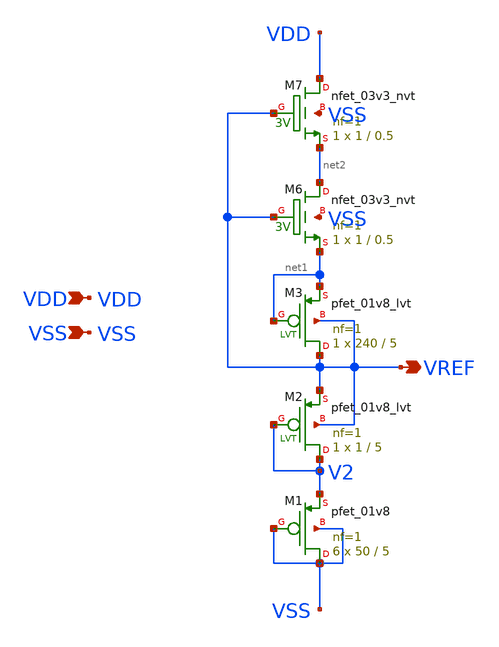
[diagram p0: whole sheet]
** sch_path: design/LELO_SVOD_SKY130A/LELO_SVOD_VTREF.sch
**.subckt LELO_SVOD_VTREF VDD VSS VREF
*.ipin VDD
*.ipin VSS
*.opin VREF
XM1 VSS VSS V2 VSS sky130_fd_pr__pfet_01v8 L=5 W=50 nf=1 ad='int((1 + 1)/2) * 50 / 1 * 0.29' as='int((1 + 2)/2) * 50 / 1 * 0.29'
+ pd='2*int((1 + 1)/2) * (50 / 1 + 0.29)' ps='2*int((1 + 2)/2) * (50 / 1 + 0.29)' nrd='0.29 / 50 ' nrs='0.29 / 50 '
+ sa=0 sb=0 sd=0 mult=6 m=6
XM2 V2 V2 VREF VREF sky130_fd_pr__pfet_01v8_lvt L=5 W=1 nf=1 ad='int((1 + 1)/2) * 1 / 1 * 0.29' as='int((1 + 2)/2) * 1 / 1 * 0.29'
+ pd='2*int((1 + 1)/2) * (1 / 1 + 0.29)' ps='2*int((1 + 2)/2) * (1 / 1 + 0.29)' nrd='0.29 / 1 ' nrs='0.29 / 1 '
+ sa=0 sb=0 sd=0 mult=1 m=1
XM3 VREF net1 net1 VREF sky130_fd_pr__pfet_01v8_lvt L=5 W=240 nf=1 ad='int((1 + 1)/2) * 240 / 1 * 0.29'
+ as='int((1 + 2)/2) * 240 / 1 * 0.29' pd='2*int((1 + 1)/2) * (240 / 1 + 0.29)' ps='2*int((1 + 2)/2) * (240 / 1 + 0.29)'
+ nrd='0.29 / 240 ' nrs='0.29 / 240 ' sa=0 sb=0 sd=0 mult=1 m=1
XM6 net2 VREF net1 VSS sky130_fd_pr__nfet_03v3_nvt L=0.5 W=1 nf=1 ad='int((1 + 1)/2) * 1 / 1 * 0.29'
+ as='int((1 + 2)/2) * 1 / 1 * 0.29' pd='2*int((1 + 1)/2) * (1 / 1 + 0.29)' ps='2*int((1 + 2)/2) * (1 / 1 + 0.29)'
+ nrd='0.29 / 1 ' nrs='0.29 / 1 ' sa=0 sb=0 sd=0 mult=1 m=1
XM7 VDD VREF net2 VSS sky130_fd_pr__nfet_03v3_nvt L=0.5 W=1 nf=1 ad='int((1 + 1)/2) * 1 / 1 * 0.29' as='int((1 + 2)/2) * 1 / 1 * 0.29'
+ pd='2*int((1 + 1)/2) * (1 / 1 + 0.29)' ps='2*int((1 + 2)/2) * (1 / 1 + 0.29)' nrd='0.29 / 1 ' nrs='0.29 / 1 '
+ sa=0 sb=0 sd=0 mult=1 m=1
**.ends
.end
